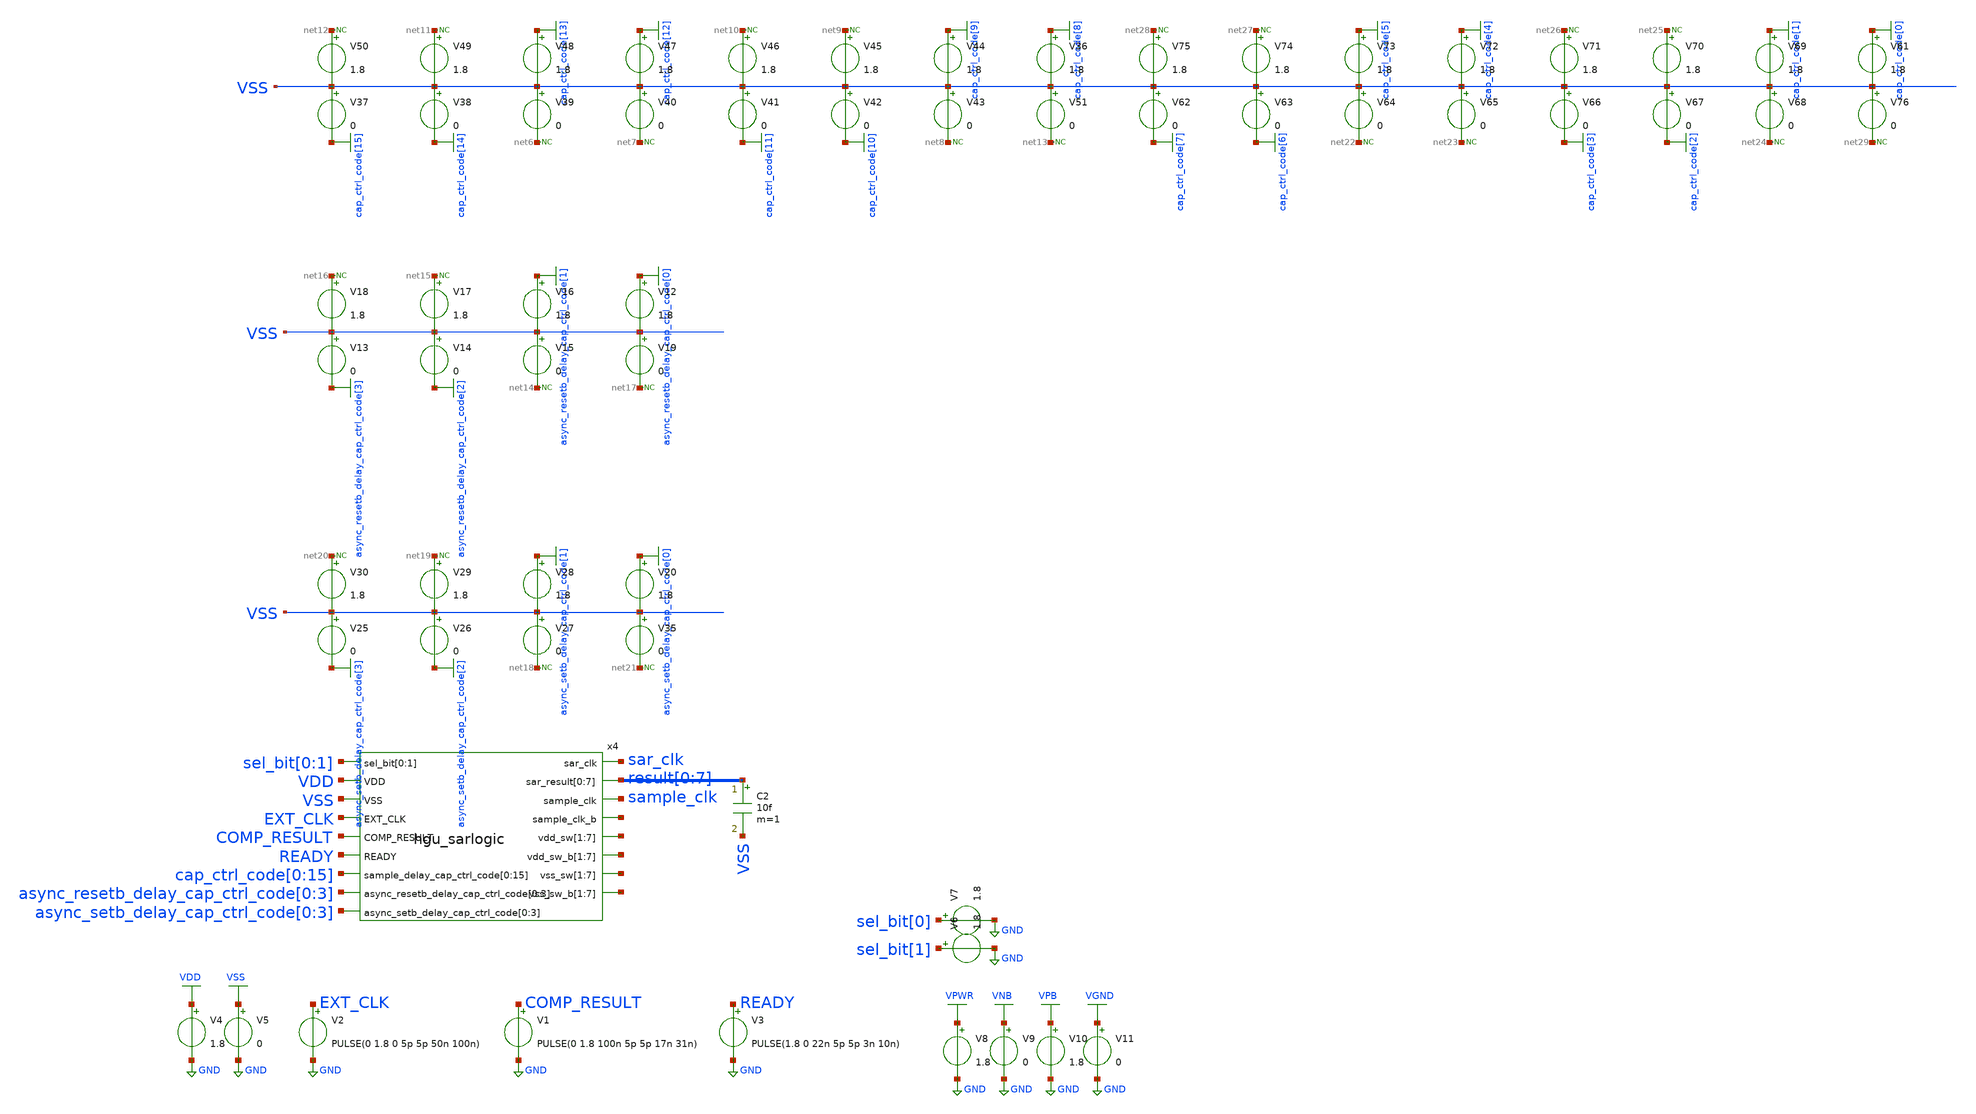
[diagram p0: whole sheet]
** sch_path: tb/tb_hgu_sarlogic_clk.sch
**.subckt tb_hgu_sarlogic_clk
V2 EXT_CLK GND PULSE(0 1.8 0 5p 5p 50n 100n)
V4 VDD GND 1.8
V1 COMP_RESULT GND PULSE(0 1.8 100n 5p 5p 17n 31n)
V5 VSS GND 0
V3 READY GND PULSE(1.8 0 22n 5p 5p 3n 10n)
x4 sar_clk result[0] result[1] result[2] result[3] result[4] result[5] result[6] result[7]
+ sample_clk sel_bit[0] sel_bit[1] net1 VDD VSS EXT_CLK COMP_RESULT READY net2[6] net2[5] net2[4] net2[3]
+ net2[2] net2[1] net2[0] net3[6] net3[5] net3[4] net3[3] net3[2] net3[1] net3[0] net4[6] net4[5] net4[4]
+ net4[3] net4[2] net4[1] net4[0] net5[6] net5[5] net5[4] net5[3] net5[2] net5[1] net5[0] cap_ctrl_code[0]
+ cap_ctrl_code[1] cap_ctrl_code[2] cap_ctrl_code[3] cap_ctrl_code[4] cap_ctrl_code[5] cap_ctrl_code[6]
+ cap_ctrl_code[7] cap_ctrl_code[8] cap_ctrl_code[9] cap_ctrl_code[10] cap_ctrl_code[11] cap_ctrl_code[12]
+ cap_ctrl_code[13] cap_ctrl_code[14] cap_ctrl_code[15] async_resetb_delay_cap_ctrl_code[0]
+ async_resetb_delay_cap_ctrl_code[1] async_resetb_delay_cap_ctrl_code[2] async_resetb_delay_cap_ctrl_code[3]
+ async_setb_delay_cap_ctrl_code[0] async_setb_delay_cap_ctrl_code[1] async_setb_delay_cap_ctrl_code[2]
+ async_setb_delay_cap_ctrl_code[3] hgu_sarlogic
C2 result[0] VSS 10f m=1
V6 sel_bit[1] GND 1.8
V7 sel_bit[0] GND 1.8
V8 VPWR GND 1.8
V9 VNB GND 0
V10 VPB GND 1.8
V11 VGND GND 0
V36 cap_ctrl_code[8] VSS 1.8
V37 VSS cap_ctrl_code[15] 0
V38 VSS cap_ctrl_code[14] 0
V39 VSS net6 0
V40 VSS net7 0
V41 VSS cap_ctrl_code[11] 0
V42 VSS cap_ctrl_code[10] 0
V43 VSS net8 0
V44 cap_ctrl_code[9] VSS 1.8
V45 net9 VSS 1.8
V46 net10 VSS 1.8
V47 cap_ctrl_code[12] VSS 1.8
V48 cap_ctrl_code[13] VSS 1.8
V49 net11 VSS 1.8
V50 net12 VSS 1.8
V51 VSS net13 0
* noconn #net12
* noconn #net11
* noconn #net6
* noconn #net7
* noconn #net10
* noconn #net9
* noconn #net8
* noconn #net13
V12 async_resetb_delay_cap_ctrl_code[0] VSS 1.8
V13 VSS async_resetb_delay_cap_ctrl_code[3] 0
V14 VSS async_resetb_delay_cap_ctrl_code[2] 0
V15 VSS net14 0
V16 async_resetb_delay_cap_ctrl_code[1] VSS 1.8
V17 net15 VSS 1.8
V18 net16 VSS 1.8
V19 VSS net17 0
* noconn #net16
* noconn #net15
* noconn #net14
* noconn #net17
V20 async_setb_delay_cap_ctrl_code[0] VSS 1.8
V25 VSS async_setb_delay_cap_ctrl_code[3] 0
V26 VSS async_setb_delay_cap_ctrl_code[2] 0
V27 VSS net18 0
V28 async_setb_delay_cap_ctrl_code[1] VSS 1.8
V29 net19 VSS 1.8
V30 net20 VSS 1.8
V35 VSS net21 0
* noconn #net20
* noconn #net19
* noconn #net18
* noconn #net21
V61 cap_ctrl_code[0] VSS 1.8
V62 VSS cap_ctrl_code[7] 0
V63 VSS cap_ctrl_code[6] 0
V64 VSS net22 0
V65 VSS net23 0
V66 VSS cap_ctrl_code[3] 0
V67 VSS cap_ctrl_code[2] 0
V68 VSS net24 0
V69 cap_ctrl_code[1] VSS 1.8
V70 net25 VSS 1.8
V71 net26 VSS 1.8
V72 cap_ctrl_code[4] VSS 1.8
V73 cap_ctrl_code[5] VSS 1.8
V74 net27 VSS 1.8
V75 net28 VSS 1.8
V76 VSS net29 0
* noconn #net28
* noconn #net27
* noconn #net22
* noconn #net23
* noconn #net26
* noconn #net25
* noconn #net24
* noconn #net29
**** begin user architecture code



.lib /foss/pdks/sky130A/libs.tech/ngspice/sky130.lib.spice tt
.include /foss/pdks/sky130A/libs.ref/sky130_fd_sc_hd/spice/sky130_fd_sc_hd.spice

.tran 10ps 400ns

.control
	option temp = 25
	let vdd_act = 1.8

	alter V4 vdd_act
	alter V8 vdd_act
	alter V10 vdd_act

	run
	plot V(EXT_CLK)-2 V(sample_clk) V(EOB)+2 V(READY)+4 V(sar_clk)+6 V(COMP_RESULT)+8
	plot V("tempD[0]") V("tempD[1]")+2 V("tempD[2]")+4 V("tempD[3]")+6 V("tempD[4]")+8 V("tempD[5]")+10
+ V("tempD[6]")+12 V("tempD[7]")+14 V(sar_clk) V(sar_clk)+2 V(sar_clk)+4 V(sar_clk)+6 V(sar_clk)+8 V(sar_clk)+10
+ V(sar_clk)+12 V(sar_clk)+14 V(EOB)-2
	plot V("result[0]") V("result[1]")+2 V("result[2]")+4 V("result[3]")+6 V("result[4]")+8
+ V("result[5]")+10 V("result[6]")+12 V("result[7]")+14
 .endc
.save all



**** end user architecture code
**.ends
.GLOBAL GND
.GLOBAL VDD
.GLOBAL VSS
.GLOBAL VGND
.GLOBAL VNB
.GLOBAL VPB
.GLOBAL VPWR
.GLOBAL cap_ctrl_code[15]
.GLOBAL cap_ctrl_code[14]
.GLOBAL cap_ctrl_code[13]
.GLOBAL cap_ctrl_code[12]
.GLOBAL cap_ctrl_code[11]
.GLOBAL cap_ctrl_code[10]
.GLOBAL cap_ctrl_code[9]
.GLOBAL cap_ctrl_code[8]
.GLOBAL async_resetb_delay_cap_ctrl_code[3]
.GLOBAL async_resetb_delay_cap_ctrl_code[2]
.GLOBAL async_resetb_delay_cap_ctrl_code[1]
.GLOBAL async_resetb_delay_cap_ctrl_code[0]
.GLOBAL async_setb_delay_cap_ctrl_code[3]
.GLOBAL async_setb_delay_cap_ctrl_code[2]
.GLOBAL async_setb_delay_cap_ctrl_code[1]
.GLOBAL async_setb_delay_cap_ctrl_code[0]
.GLOBAL cap_ctrl_code[7]
.GLOBAL cap_ctrl_code[6]
.GLOBAL cap_ctrl_code[5]
.GLOBAL cap_ctrl_code[4]
.GLOBAL cap_ctrl_code[3]
.GLOBAL cap_ctrl_code[2]
.GLOBAL cap_ctrl_code[1]
.GLOBAL cap_ctrl_code[0]
.end
